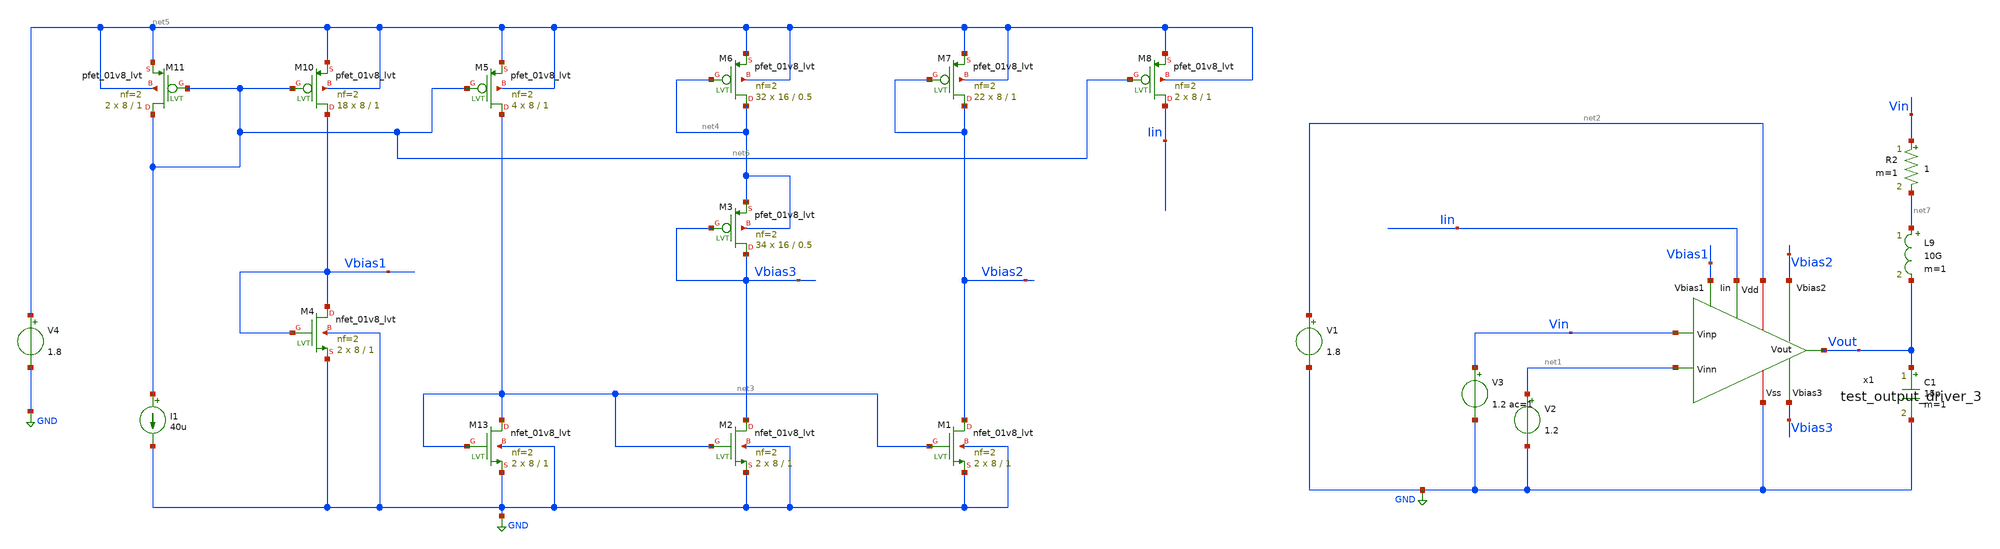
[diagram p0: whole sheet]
** sch_path: xschem/ip_block/opamp/folded_cas_xiaoyi/tb_test_output_driver_3.sch
**.subckt tb_test_output_driver_3
V1 net2 GND 1.8
V2 net1 GND 1.2
V3 Vin GND 1.2 ac=1
C1 Vout GND 15p m=1
XM2 Vbias3 net3 GND GND sky130_fd_pr__nfet_01v8_lvt L=1 W=8 nf=2 ad='int((nf+1)/2) * W/nf * 0.29' as='int((nf+2)/2) * W/nf * 0.29'
+ pd='2*int((nf+1)/2) * (W/nf + 0.29)' ps='2*int((nf+2)/2) * (W/nf + 0.29)' nrd='0.29 / W' nrs='0.29 / W'
+ sa=0 sb=0 sd=0 mult=2 m=2
XM3 Vbias3 Vbias3 net4 net4 sky130_fd_pr__pfet_01v8_lvt L=0.5 W=16 nf=2 ad='int((nf+1)/2) * W/nf * 0.29'
+ as='int((nf+2)/2) * W/nf * 0.29' pd='2*int((nf+1)/2) * (W/nf + 0.29)' ps='2*int((nf+2)/2) * (W/nf + 0.29)'
+ nrd='0.29 / W' nrs='0.29 / W' sa=0 sb=0 sd=0 mult=34 m=34
I1 net6 GND 40u
XM4 Vbias1 Vbias1 GND GND sky130_fd_pr__nfet_01v8_lvt L=1 W=8 nf=2 ad='int((nf+1)/2) * W/nf * 0.29' as='int((nf+2)/2) * W/nf * 0.29'
+ pd='2*int((nf+1)/2) * (W/nf + 0.29)' ps='2*int((nf+2)/2) * (W/nf + 0.29)' nrd='0.29 / W' nrs='0.29 / W'
+ sa=0 sb=0 sd=0 mult=2 m=2
V4 net5 GND 1.8
XM1 Vbias2 net3 GND GND sky130_fd_pr__nfet_01v8_lvt L=1 W=8 nf=2 ad='int((nf+1)/2) * W/nf * 0.29' as='int((nf+2)/2) * W/nf * 0.29'
+ pd='2*int((nf+1)/2) * (W/nf + 0.29)' ps='2*int((nf+2)/2) * (W/nf + 0.29)' nrd='0.29 / W' nrs='0.29 / W'
+ sa=0 sb=0 sd=0 mult=2 m=2
XM6 net4 net4 net5 net5 sky130_fd_pr__pfet_01v8_lvt L=0.5 W=16 nf=2 ad='int((nf+1)/2) * W/nf * 0.29'
+ as='int((nf+2)/2) * W/nf * 0.29' pd='2*int((nf+1)/2) * (W/nf + 0.29)' ps='2*int((nf+2)/2) * (W/nf + 0.29)'
+ nrd='0.29 / W' nrs='0.29 / W' sa=0 sb=0 sd=0 mult=32 m=32
XM7 Vbias2 Vbias2 net5 net5 sky130_fd_pr__pfet_01v8_lvt L=1 W=8 nf=2 ad='int((nf+1)/2) * W/nf * 0.29'
+ as='int((nf+2)/2) * W/nf * 0.29' pd='2*int((nf+1)/2) * (W/nf + 0.29)' ps='2*int((nf+2)/2) * (W/nf + 0.29)'
+ nrd='0.29 / W' nrs='0.29 / W' sa=0 sb=0 sd=0 mult=22 m=22
XM5 net3 net6 net5 net5 sky130_fd_pr__pfet_01v8_lvt L=1 W=8 nf=2 ad='int((nf+1)/2) * W/nf * 0.29' as='int((nf+2)/2) * W/nf * 0.29'
+ pd='2*int((nf+1)/2) * (W/nf + 0.29)' ps='2*int((nf+2)/2) * (W/nf + 0.29)' nrd='0.29 / W' nrs='0.29 / W'
+ sa=0 sb=0 sd=0 mult=4 m=4
XM10 Vbias1 net6 net5 net5 sky130_fd_pr__pfet_01v8_lvt L=1 W=8 nf=2 ad='int((nf+1)/2) * W/nf * 0.29'
+ as='int((nf+2)/2) * W/nf * 0.29' pd='2*int((nf+1)/2) * (W/nf + 0.29)' ps='2*int((nf+2)/2) * (W/nf + 0.29)'
+ nrd='0.29 / W' nrs='0.29 / W' sa=0 sb=0 sd=0 mult=18 m=18
XM11 net6 net6 net5 net5 sky130_fd_pr__pfet_01v8_lvt L=1 W=8 nf=2 ad='int((nf+1)/2) * W/nf * 0.29' as='int((nf+2)/2) * W/nf * 0.29'
+ pd='2*int((nf+1)/2) * (W/nf + 0.29)' ps='2*int((nf+2)/2) * (W/nf + 0.29)' nrd='0.29 / W' nrs='0.29 / W'
+ sa=0 sb=0 sd=0 mult=2 m=2
XM13 net3 net3 GND GND sky130_fd_pr__nfet_01v8_lvt L=1 W=8 nf=2 ad='int((nf+1)/2) * W/nf * 0.29' as='int((nf+2)/2) * W/nf * 0.29'
+ pd='2*int((nf+1)/2) * (W/nf + 0.29)' ps='2*int((nf+2)/2) * (W/nf + 0.29)' nrd='0.29 / W' nrs='0.29 / W'
+ sa=0 sb=0 sd=0 mult=2 m=2
x1 net2 net1 Vin Vout Iin GND Vbias1 Vbias2 Vbias3 test_output_driver_3
L9 net7 Vout 10G m=1
R2 Vin net7 1 m=1
XM8 Iin net6 net5 net5 sky130_fd_pr__pfet_01v8_lvt L=1 W=8 nf=2 ad='int((nf+1)/2) * W/nf * 0.29' as='int((nf+2)/2) * W/nf * 0.29'
+ pd='2*int((nf+1)/2) * (W/nf + 0.29)' ps='2*int((nf+2)/2) * (W/nf + 0.29)' nrd='0.29 / W' nrs='0.29 / W'
+ sa=0 sb=0 sd=0 mult=2 m=2
**** begin user architecture code
.lib $::SKYWATER_MODELS/sky130.lib.spice tt


.option temp=70
.op
.ac dec 10 1 1G
*.tran 0.1n 100u

.control
ac dec 10 1 1G
*tran 0.1n 100u
*ac dec 10 1 1G
let phase = 180/PI*vp(Vout)

plot vdb(Vout) phase
*plot Vin_p Vout
.endc

.save all



**** end user architecture code
**.ends
.GLOBAL GND
.end
